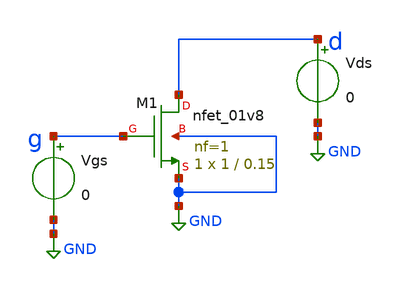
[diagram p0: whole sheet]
** sch_path: xschem/nmos_char.sch
**.subckt nmos_char
XM1 d g GND GND sky130_fd_pr__nfet_01v8 L=0.15 W=1 nf=1 ad='int((nf+1)/2) * W/nf * 0.29' as='int((nf+2)/2) * W/nf * 0.29'
+ pd='2*int((nf+1)/2) * (W/nf + 0.29)' ps='2*int((nf+2)/2) * (W/nf + 0.29)' nrd='0.29 / W' nrs='0.29 / W'
+ sa=0 sb=0 sd=0 mult=1 m=1
Vgs g GND 0
Vds d GND 0
**** begin user architecture code
 .lib $::SKYWATER_MODELS/sky130.lib.spice tt


.dc Vds 0 1.8 1m Vgs 0 2 0.5
.save all


**** end user architecture code
**.ends
.GLOBAL GND
.end
